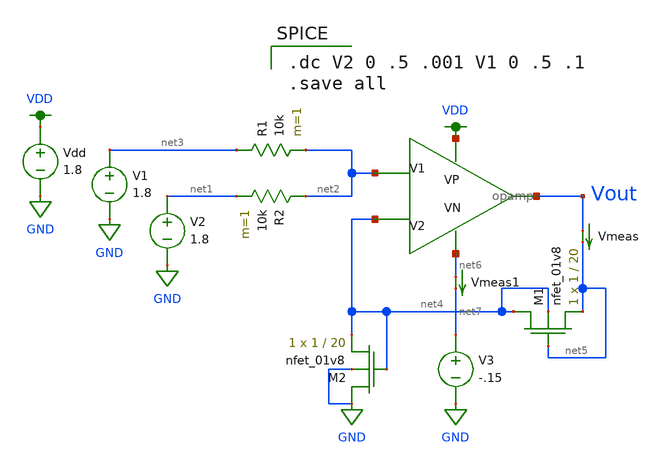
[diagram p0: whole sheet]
** sch_path: schematics/old/opamp_adder_testbench.sch
**.subckt opamp_adder_testbench
Vdd VDD GND 1.8
X1 net2 net4 VDD net6 Vout opamp
V1 net3 GND 1.8
V2 net1 GND 1.8
XM1 net4 net5 net5 net4 sky130_fd_pr__nfet_01v8 L=20 W=1 nf=1 ad='int((nf+1)/2) * W/nf * 0.29' as='int((nf+2)/2) * W/nf * 0.29'
+ pd='2*int((nf+1)/2) * (W/nf + 0.29)' ps='2*int((nf+2)/2) * (W/nf + 0.29)' nrd='0.29 / W' nrs='0.29 / W'
+ sa=0 sb=0 sd=0 mult=1 m=1
XM2 GND net4 net4 GND sky130_fd_pr__nfet_01v8 L=20 W=1 nf=1 ad='int((nf+1)/2) * W/nf * 0.29' as='int((nf+2)/2) * W/nf * 0.29'
+ pd='2*int((nf+1)/2) * (W/nf + 0.29)' ps='2*int((nf+2)/2) * (W/nf + 0.29)' nrd='0.29 / W' nrs='0.29 / W'
+ sa=0 sb=0 sd=0 mult=1 m=1
Vmeas Vout net5 0
.save i(vmeas)
R1 net3 net2 10k m=1
R2 net2 net1 10k m=1
V3 net7 GND -.15
Vmeas1 net6 net7 0
.save i(vmeas1)
**** begin user architecture code

.option wnflag=1
.lib ~/skywater/skywater-pdk/libraries/sky130_fd_pr_ngspice/latest/models/sky130.lib.spice tt


.dc V2 0 .5 .001 V1 0 .5 .1
.save all

**** end user architecture code
**.ends

* expanding   symbol:  /home/madvlsi/Documents/MADVLSI_final/schematics/opamp.sym # of pins=5
** sym_path: schematics/opamp.sym
** sch_path: schematics/opamp.sch
.subckt opamp V1 V2 VP VN Vout
*.ipin V1
*.ipin V2
*.opin Vout
*.iopin VP
*.iopin VN
*.iopin VP
*.iopin VN
XM1 VN net7 net2 GND sky130_fd_pr__nfet_01v8 L=l W=w nf=1 ad='int((nf+1)/2) * W/nf * 0.29' as='int((nf+2)/2) * W/nf * 0.29'
+ pd='2*int((nf+1)/2) * (W/nf + 0.29)' ps='2*int((nf+2)/2) * (W/nf + 0.29)' nrd='0.29 / W' nrs='0.29 / W'
+ sa=0 sb=0 sd=0 mult=1 m=1
XM2 VP net3 net1 VDD sky130_fd_pr__pfet_01v8 L=l W=w nf=1 ad='int((nf+1)/2) * W/nf * 0.29' as='int((nf+2)/2) * W/nf * 0.29'
+ pd='2*int((nf+1)/2) * (W/nf + 0.29)' ps='2*int((nf+2)/2) * (W/nf + 0.29)' nrd='0.29 / W' nrs='0.29 / W'
+ sa=0 sb=0 sd=0 mult=1 m=1
XM3 net1 V1 Vd VDD sky130_fd_pr__pfet_01v8 L=l W=w nf=1 ad='int((nf+1)/2) * W/nf * 0.29' as='int((nf+2)/2) * W/nf * 0.29'
+ pd='2*int((nf+1)/2) * (W/nf + 0.29)' ps='2*int((nf+2)/2) * (W/nf + 0.29)' nrd='0.29 / W' nrs='0.29 / W'
+ sa=0 sb=0 sd=0 mult=1 m=1
XM4 Vc V2 net1 VDD sky130_fd_pr__pfet_01v8 L=l W=w nf=1 ad='int((nf+1)/2) * W/nf * 0.29' as='int((nf+2)/2) * W/nf * 0.29'
+ pd='2*int((nf+1)/2) * (W/nf + 0.29)' ps='2*int((nf+2)/2) * (W/nf + 0.29)' nrd='0.29 / W' nrs='0.29 / W'
+ sa=0 sb=0 sd=0 mult=1 m=1
XM5 Va V2 net2 GND sky130_fd_pr__nfet_01v8 L=l W=w nf=1 ad='int((nf+1)/2) * W/nf * 0.29' as='int((nf+2)/2) * W/nf * 0.29'
+ pd='2*int((nf+1)/2) * (W/nf + 0.29)' ps='2*int((nf+2)/2) * (W/nf + 0.29)' nrd='0.29 / W' nrs='0.29 / W'
+ sa=0 sb=0 sd=0 mult=1 m=1
XM6 net2 V1 Vb GND sky130_fd_pr__nfet_01v8 L=l W=w nf=1 ad='int((nf+1)/2) * W/nf * 0.29' as='int((nf+2)/2) * W/nf * 0.29'
+ pd='2*int((nf+1)/2) * (W/nf + 0.29)' ps='2*int((nf+2)/2) * (W/nf + 0.29)' nrd='0.29 / W' nrs='0.29 / W'
+ sa=0 sb=0 sd=0 mult=1 m=1
XM7 net3 net3 Va VDD sky130_fd_pr__pfet_01v8 L=l W=w nf=1 ad='int((nf+1)/2) * W/nf * 0.29' as='int((nf+2)/2) * W/nf * 0.29'
+ pd='2*int((nf+1)/2) * (W/nf + 0.29)' ps='2*int((nf+2)/2) * (W/nf + 0.29)' nrd='0.29 / W' nrs='0.29 / W'
+ sa=0 sb=0 sd=0 mult=1 m=1
XM8 net6 net6 Va VDD sky130_fd_pr__pfet_01v8 L=l W=w nf=1 ad='int((nf+1)/2) * W/nf * 0.29' as='int((nf+2)/2) * W/nf * 0.29'
+ pd='2*int((nf+1)/2) * (W/nf + 0.29)' ps='2*int((nf+2)/2) * (W/nf + 0.29)' nrd='0.29 / W' nrs='0.29 / W'
+ sa=0 sb=0 sd=0 mult=1 m=1
XM9 net5 net6 Vb VDD sky130_fd_pr__pfet_01v8 L=l W=w nf=1 ad='int((nf+1)/2) * W/nf * 0.29' as='int((nf+2)/2) * W/nf * 0.29'
+ pd='2*int((nf+1)/2) * (W/nf + 0.29)' ps='2*int((nf+2)/2) * (W/nf + 0.29)' nrd='0.29 / W' nrs='0.29 / W'
+ sa=0 sb=0 sd=0 mult=1 m=1
XM10 Va net3 VP VDD sky130_fd_pr__pfet_01v8 L=l W=w nf=1 ad='int((nf+1)/2) * W/nf * 0.29' as='int((nf+2)/2) * W/nf * 0.29'
+ pd='2*int((nf+1)/2) * (W/nf + 0.29)' ps='2*int((nf+2)/2) * (W/nf + 0.29)' nrd='0.29 / W' nrs='0.29 / W'
+ sa=0 sb=0 sd=0 mult=1 m=1
XM11 Vb net3 VP VDD sky130_fd_pr__pfet_01v8 L=l W=w nf=1 ad='int((nf+1)/2) * W/nf * 0.29' as='int((nf+2)/2) * W/nf * 0.29'
+ pd='2*int((nf+1)/2) * (W/nf + 0.29)' ps='2*int((nf+2)/2) * (W/nf + 0.29)' nrd='0.29 / W' nrs='0.29 / W'
+ sa=0 sb=0 sd=0 mult=1 m=1
XM12 net6 net6 Vc GND sky130_fd_pr__nfet_01v8 L=l W=w nf=1 ad='int((nf+1)/2) * W/nf * 0.29' as='int((nf+2)/2) * W/nf * 0.29'
+ pd='2*int((nf+1)/2) * (W/nf + 0.29)' ps='2*int((nf+2)/2) * (W/nf + 0.29)' nrd='0.29 / W' nrs='0.29 / W'
+ sa=0 sb=0 sd=0 mult=1 m=1
XM13 net5 net6 Vd GND sky130_fd_pr__nfet_01v8 L=l W=w nf=1 ad='int((nf+1)/2) * W/nf * 0.29' as='int((nf+2)/2) * W/nf * 0.29'
+ pd='2*int((nf+1)/2) * (W/nf + 0.29)' ps='2*int((nf+2)/2) * (W/nf + 0.29)' nrd='0.29 / W' nrs='0.29 / W'
+ sa=0 sb=0 sd=0 mult=1 m=1
XM14 Vc net7 VN GND sky130_fd_pr__nfet_01v8 L=l W=w nf=1 ad='int((nf+1)/2) * W/nf * 0.29' as='int((nf+2)/2) * W/nf * 0.29'
+ pd='2*int((nf+1)/2) * (W/nf + 0.29)' ps='2*int((nf+2)/2) * (W/nf + 0.29)' nrd='0.29 / W' nrs='0.29 / W'
+ sa=0 sb=0 sd=0 mult=1 m=1
XM15 Vd net7 VN GND sky130_fd_pr__nfet_01v8 L=l W=w nf=1 ad='int((nf+1)/2) * W/nf * 0.29' as='int((nf+2)/2) * W/nf * 0.29'
+ pd='2*int((nf+1)/2) * (W/nf + 0.29)' ps='2*int((nf+2)/2) * (W/nf + 0.29)' nrd='0.29 / W' nrs='0.29 / W'
+ sa=0 sb=0 sd=0 mult=1 m=1
XM16 net8 net7 net3 GND sky130_fd_pr__nfet_01v8 L=l W=w nf=1 ad='int((nf+1)/2) * W/nf * 0.29' as='int((nf+2)/2) * W/nf * 0.29'
+ pd='2*int((nf+1)/2) * (W/nf + 0.29)' ps='2*int((nf+2)/2) * (W/nf + 0.29)' nrd='0.29 / W' nrs='0.29 / W'
+ sa=0 sb=0 sd=0 mult=1 m=1
XM17 VN net7 net8 GND sky130_fd_pr__nfet_01v8 L=l W=w nf=1 ad='int((nf+1)/2) * W/nf * 0.29' as='int((nf+2)/2) * W/nf * 0.29'
+ pd='2*int((nf+1)/2) * (W/nf + 0.29)' ps='2*int((nf+2)/2) * (W/nf + 0.29)' nrd='0.29 / W' nrs='0.29 / W'
+ sa=0 sb=0 sd=0 mult=1 m=1
XM18 net8 net7 VP GND sky130_fd_pr__nfet_01v8 L=l W=w nf=1 ad='int((nf+1)/2) * W/nf * 0.29' as='int((nf+2)/2) * W/nf * 0.29'
+ pd='2*int((nf+1)/2) * (W/nf + 0.29)' ps='2*int((nf+2)/2) * (W/nf + 0.29)' nrd='0.29 / W' nrs='0.29 / W'
+ sa=0 sb=0 sd=0 mult=M m=M
XM19 net4 net3 net7 VDD sky130_fd_pr__pfet_01v8 L=l W=w nf=1 ad='int((nf+1)/2) * W/nf * 0.29' as='int((nf+2)/2) * W/nf * 0.29'
+ pd='2*int((nf+1)/2) * (W/nf + 0.29)' ps='2*int((nf+2)/2) * (W/nf + 0.29)' nrd='0.29 / W' nrs='0.29 / W'
+ sa=0 sb=0 sd=0 mult=1 m=1
XM20 VP net3 net4 VDD sky130_fd_pr__pfet_01v8 L=l W=w nf=1 ad='int((nf+1)/2) * W/nf * 0.29' as='int((nf+2)/2) * W/nf * 0.29'
+ pd='2*int((nf+1)/2) * (W/nf + 0.29)' ps='2*int((nf+2)/2) * (W/nf + 0.29)' nrd='0.29 / W' nrs='0.29 / W'
+ sa=0 sb=0 sd=0 mult=1 m=1
XM21 net4 net3 VN VDD sky130_fd_pr__pfet_01v8 L=l W=w nf=1 ad='int((nf+1)/2) * W/nf * 0.29' as='int((nf+2)/2) * W/nf * 0.29'
+ pd='2*int((nf+1)/2) * (W/nf + 0.29)' ps='2*int((nf+2)/2) * (W/nf + 0.29)' nrd='0.29 / W' nrs='0.29 / W'
+ sa=0 sb=0 sd=0 mult=M m=M
XM22 net7 net7 Vc GND sky130_fd_pr__nfet_01v8 L=l W=w nf=1 ad='int((nf+1)/2) * W/nf * 0.29' as='int((nf+2)/2) * W/nf * 0.29'
+ pd='2*int((nf+1)/2) * (W/nf + 0.29)' ps='2*int((nf+2)/2) * (W/nf + 0.29)' nrd='0.29 / W' nrs='0.29 / W'
+ sa=0 sb=0 sd=0 mult=1 m=1
**** begin user architecture code

.param M=3
.param w=3
.param l=0.6


**** end user architecture code
XM23 Vout net5 VN GND sky130_fd_pr__nfet_01v8 L=.15 W=6 nf=1 ad='int((nf+1)/2) * W/nf * 0.29' as='int((nf+2)/2) * W/nf * 0.29'
+ pd='2*int((nf+1)/2) * (W/nf + 0.29)' ps='2*int((nf+2)/2) * (W/nf + 0.29)' nrd='0.29 / W' nrs='0.29 / W'
+ sa=0 sb=0 sd=0 mult=1 m=1
XM24 Vout net5 VP VDD sky130_fd_pr__pfet_01v8 L=.15 W=12 nf=1 ad='int((nf+1)/2) * W/nf * 0.29' as='int((nf+2)/2) * W/nf * 0.29'
+ pd='2*int((nf+1)/2) * (W/nf + 0.29)' ps='2*int((nf+2)/2) * (W/nf + 0.29)' nrd='0.29 / W' nrs='0.29 / W'
+ sa=0 sb=0 sd=0 mult=1 m=1
C1 Vout net5 500f m=1
.ends

.GLOBAL VDD
.GLOBAL GND
.end
